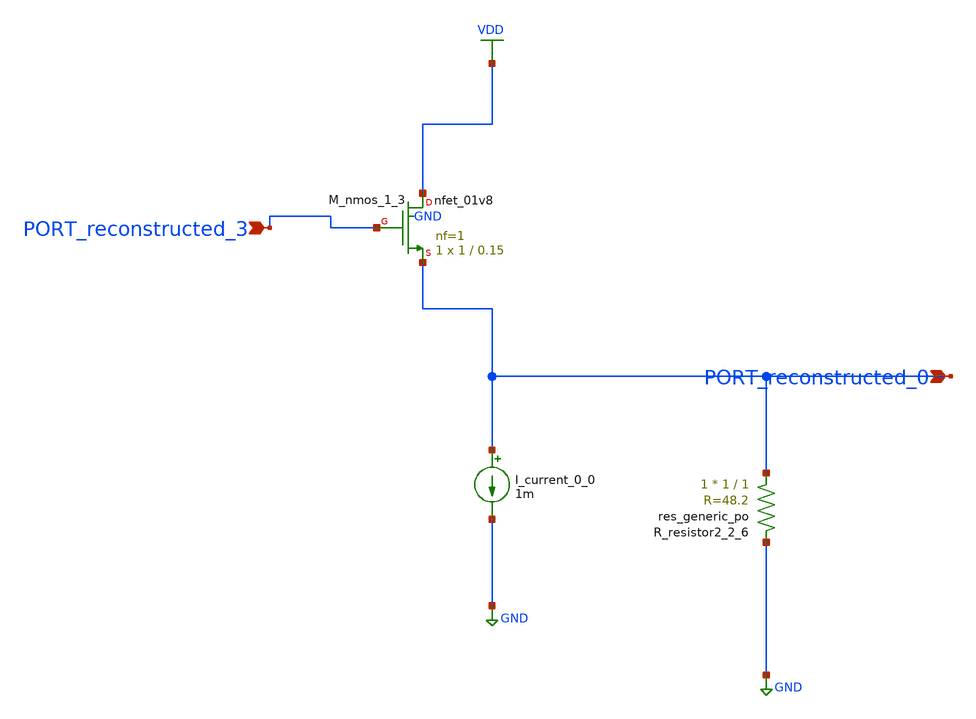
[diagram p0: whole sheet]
** sch_path: schematics/AMSNet/108.sch
**.subckt 108 PORT_reconstructed_3 PORT_reconstructed_0
*.ipin PORT_reconstructed_3
*.ipin PORT_reconstructed_0
I_current_0_0 PORT_reconstructed_0 GND 1m
XM_nmos_1_3 VDD PORT_reconstructed_3 PORT_reconstructed_0 GND sky130_fd_pr__nfet_01v8 L=0.15 W=1 nf=1
+ ad='int((1 + 1)/2) * 1 / 1 * 0.29' as='int((1 + 2)/2) * 1 / 1 * 0.29' pd='2*int((1 + 1)/2) * (1 / 1 + 0.29)'
+ ps='2*int((1 + 2)/2) * (1 / 1 + 0.29)' nrd='0.29 / 1 ' nrs='0.29 / 1 ' sa=0 sb=0 sd=0 mult=1 m=1
XR_resistor2_2_6 PORT_reconstructed_0 GND sky130_fd_pr__res_generic_po W=1 L=1 m=1
**.ends
.GLOBAL GND
.GLOBAL VDD
.end
